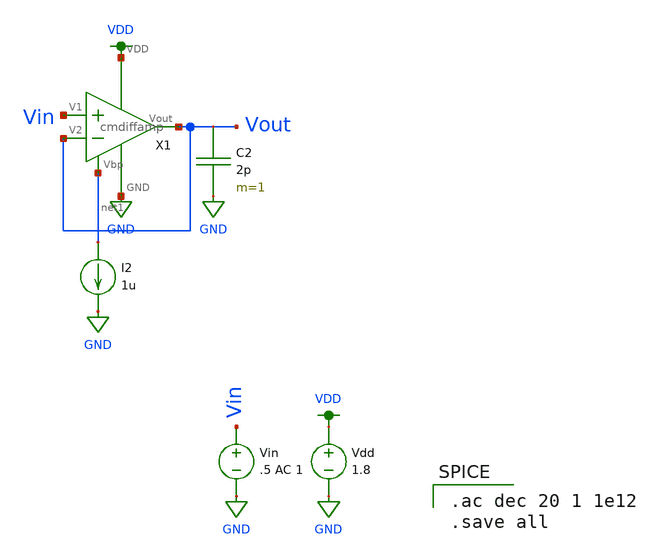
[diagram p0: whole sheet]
** sch_path: Miniproject3/SImulations/unity_gain_follower_frequency_response_sim.sch
**.subckt unity_gain_follower_frequency_response_sim
Vdd VDD GND 1.8
I2 net1 GND 1u
C2 Vout GND 2p m=1
X1 Vout GND VDD Vin Vout net1 cmdiffamp
Vin Vin GND .5 AC 1
**** begin user architecture code

.option wnflag=1
.lib ~/skywater/skywater-pdk/libraries/sky130_fd_pr_ngspice/latest/models/sky130.lib.spice tt


.ac dec 20 1 1e12
.save all

**** end user architecture code
**.ends
.GLOBAL VDD
.GLOBAL GND
.end
